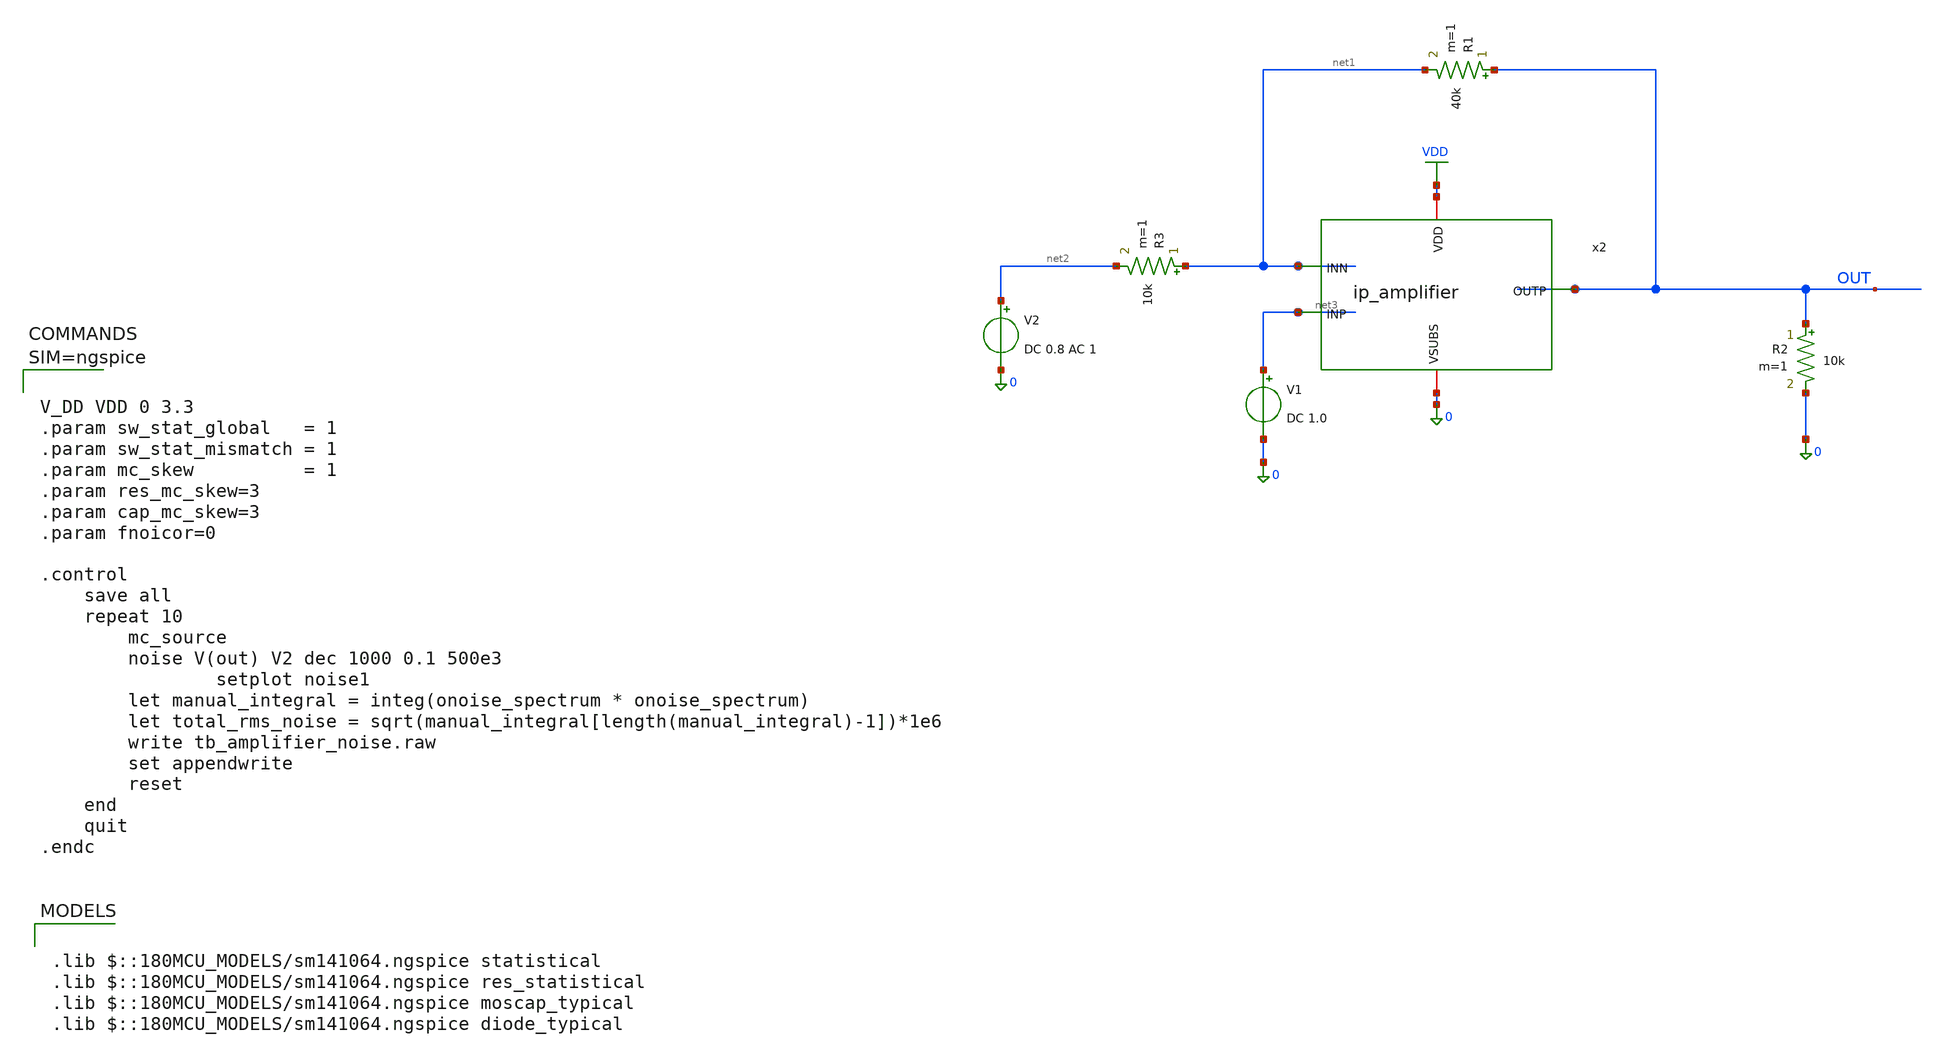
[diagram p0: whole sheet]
** sch_path: xschem/tb_amplifier_noise.sch
**.subckt tb_amplifier_noise
V2 net2 0 DC 0.8 AC 1
x2 VDD OUT net3 net1 0 ip_amplifier
R2 OUT 0 10k m=1
R1 OUT net1 40k m=1
R3 net1 net2 10k m=1
V1 net3 0 DC 1.0
**** begin user architecture code

.lib $::180MCU_MODELS/sm141064.ngspice statistical
.lib $::180MCU_MODELS/sm141064.ngspice res_statistical
.lib $::180MCU_MODELS/sm141064.ngspice moscap_typical
.lib $::180MCU_MODELS/sm141064.ngspice diode_typical




V_DD VDD 0 3.3
.param sw_stat_global   = 1
.param sw_stat_mismatch = 1
.param mc_skew          = 1
.param res_mc_skew=3
.param cap_mc_skew=3
.param fnoicor=0

.control
	save all
	repeat 10
		mc_source
		noise V(out) V2 dec 1000 0.1 500e3
                setplot noise1
		let manual_integral = integ(onoise_spectrum * onoise_spectrum)
		let total_rms_noise = sqrt(manual_integral[length(manual_integral)-1])*1e6
		write tb_amplifier_noise.raw
		set appendwrite
		reset
	end
	quit
.endc



**** end user architecture code
**.ends

* expanding   symbol:  ip_amplifier.sym # of pins=5
** sym_path: xschem/ip_amplifier.sym
** sch_path: xschem/ip_amplifier.sch
.subckt ip_amplifier VDD OUTP INP INN VSUBS
*.iopin VDD
*.iopin VSUBS
*.ipin INP
*.ipin INN
*.opin OUTP
XM1 net10 INP net8 VDD pfet_06v0 L=0.7u W=7.0u nf=1 ad='int((nf+1)/2) * W/nf * 0.18u' as='int((nf+2)/2) * W/nf * 0.18u'
+ pd='2*int((nf+1)/2) * (W/nf + 0.18u)' ps='2*int((nf+2)/2) * (W/nf + 0.18u)' nrd='0.18u / W' nrs='0.18u / W'
+ sa=0 sb=0 sd=0 m=3 par=3
XM2 net9 INN net8 VDD pfet_06v0 L=0.7u W=7.0u nf=1 ad='int((nf+1)/2) * W/nf * 0.18u' as='int((nf+2)/2) * W/nf * 0.18u'
+ pd='2*int((nf+1)/2) * (W/nf + 0.18u)' ps='2*int((nf+2)/2) * (W/nf + 0.18u)' nrd='0.18u / W' nrs='0.18u / W'
+ sa=0 sb=0 sd=0 m=3 par=3
XM5 net10 net1 VSUBS vsubs nfet_06v0 L=2u W=5u nf=1 ad='int((nf+1)/2) * W/nf * 0.18u' as='int((nf+2)/2) * W/nf * 0.18u'
+ pd='2*int((nf+1)/2) * (W/nf + 0.18u)' ps='2*int((nf+2)/2) * (W/nf + 0.18u)' nrd='0.18u / W' nrs='0.18u / W'
+ sa=0 sb=0 sd=0 m=1 par=1
XM6 net9 net1 VSUBS vsubs nfet_06v0 L=2u W=5u nf=1 ad='int((nf+1)/2) * W/nf * 0.18u' as='int((nf+2)/2) * W/nf * 0.18u'
+ pd='2*int((nf+1)/2) * (W/nf + 0.18u)' ps='2*int((nf+2)/2) * (W/nf + 0.18u)' nrd='0.18u / W' nrs='0.18u / W'
+ sa=0 sb=0 sd=0 m=1 par=1
XM3 net3 net1 VSUBS vsubs nfet_06v0 L=1u W=5u nf=1 ad='int((nf+1)/2) * W/nf * 0.18u' as='int((nf+2)/2) * W/nf * 0.18u'
+ pd='2*int((nf+1)/2) * (W/nf + 0.18u)' ps='2*int((nf+2)/2) * (W/nf + 0.18u)' nrd='0.18u / W' nrs='0.18u / W'
+ sa=0 sb=0 sd=0 m=5 par=5
XM4 net2 net1 VSUBS vsubs nfet_06v0 L=1u W=5u nf=1 ad='int((nf+1)/2) * W/nf * 0.18u' as='int((nf+2)/2) * W/nf * 0.18u'
+ pd='2*int((nf+1)/2) * (W/nf + 0.18u)' ps='2*int((nf+2)/2) * (W/nf + 0.18u)' nrd='0.18u / W' nrs='0.18u / W'
+ sa=0 sb=0 sd=0 m=1 par=1
XM7 net1 net1 net3 vsubs nfet_06v0 L=0.7u W=5u nf=1 ad='int((nf+1)/2) * W/nf * 0.18u' as='int((nf+2)/2) * W/nf * 0.18u'
+ pd='2*int((nf+1)/2) * (W/nf + 0.18u)' ps='2*int((nf+2)/2) * (W/nf + 0.18u)' nrd='0.18u / W' nrs='0.18u / W'
+ sa=0 sb=0 sd=0 m=7 par=7
XM8 net4 net1 net2 vsubs nfet_06v0 L=0.7u W=5u nf=1 ad='int((nf+1)/2) * W/nf * 0.18u' as='int((nf+2)/2) * W/nf * 0.18u'
+ pd='2*int((nf+1)/2) * (W/nf + 0.18u)' ps='2*int((nf+2)/2) * (W/nf + 0.18u)' nrd='0.18u / W' nrs='0.18u / W'
+ sa=0 sb=0 sd=0 m=7 par=7
XM9 net5 net7 VDD VDD pfet_06v0 L=1u W=6u nf=1 ad='int((nf+1)/2) * W/nf * 0.18u' as='int((nf+2)/2) * W/nf * 0.18u'
+ pd='2*int((nf+1)/2) * (W/nf + 0.18u)' ps='2*int((nf+2)/2) * (W/nf + 0.18u)' nrd='0.18u / W' nrs='0.18u / W'
+ sa=0 sb=0 sd=0 m=1 par=1
XM10 net6 net7 VDD VDD pfet_06v0 L=1u W=6u nf=1 ad='int((nf+1)/2) * W/nf * 0.18u' as='int((nf+2)/2) * W/nf * 0.18u'
+ pd='2*int((nf+1)/2) * (W/nf + 0.18u)' ps='2*int((nf+2)/2) * (W/nf + 0.18u)' nrd='0.18u / W' nrs='0.18u / W'
+ sa=0 sb=0 sd=0 m=1 par=1
XM11 net7 net7 net5 VDD pfet_06v0 L=0.7u W=7u nf=1 ad='int((nf+1)/2) * W/nf * 0.18u' as='int((nf+2)/2) * W/nf * 0.18u'
+ pd='2*int((nf+1)/2) * (W/nf + 0.18u)' ps='2*int((nf+2)/2) * (W/nf + 0.18u)' nrd='0.18u / W' nrs='0.18u / W'
+ sa=0 sb=0 sd=0 m=5 par=5
XM12 net8 net7 net6 VDD pfet_06v0 L=0.7u W=7u nf=1 ad='int((nf+1)/2) * W/nf * 0.18u' as='int((nf+2)/2) * W/nf * 0.18u'
+ pd='2*int((nf+1)/2) * (W/nf + 0.18u)' ps='2*int((nf+2)/2) * (W/nf + 0.18u)' nrd='0.18u / W' nrs='0.18u / W'
+ sa=0 sb=0 sd=0 m=5 par=5
XM13 net11 net1 net9 vsubs nfet_06v0 L=0.7u W=7u nf=1 ad='int((nf+1)/2) * W/nf * 0.18u' as='int((nf+2)/2) * W/nf * 0.18u'
+ pd='2*int((nf+1)/2) * (W/nf + 0.18u)' ps='2*int((nf+2)/2) * (W/nf + 0.18u)' nrd='0.18u / W' nrs='0.18u / W'
+ sa=0 sb=0 sd=0 m=1 par=1
XM14 COMP net1 net10 vsubs nfet_06v0 L=0.7u W=7u nf=1 ad='int((nf+1)/2) * W/nf * 0.18u' as='int((nf+2)/2) * W/nf * 0.18u'
+ pd='2*int((nf+1)/2) * (W/nf + 0.18u)' ps='2*int((nf+2)/2) * (W/nf + 0.18u)' nrd='0.18u / W' nrs='0.18u / W'
+ sa=0 sb=0 sd=0 m=1 par=1
XM15 net11 net11 VDD VDD pfet_06v0 L=0.7u W=7u nf=1 ad='int((nf+1)/2) * W/nf * 0.18u' as='int((nf+2)/2) * W/nf * 0.18u'
+ pd='2*int((nf+1)/2) * (W/nf + 0.18u)' ps='2*int((nf+2)/2) * (W/nf + 0.18u)' nrd='0.18u / W' nrs='0.18u / W'
+ sa=0 sb=0 sd=0 m=1 par=1
XM16 COMP net11 VDD VDD pfet_06v0 L=0.7u W=7u nf=1 ad='int((nf+1)/2) * W/nf * 0.18u' as='int((nf+2)/2) * W/nf * 0.18u'
+ pd='2*int((nf+1)/2) * (W/nf + 0.18u)' ps='2*int((nf+2)/2) * (W/nf + 0.18u)' nrd='0.18u / W' nrs='0.18u / W'
+ sa=0 sb=0 sd=0 m=1 par=1
XM17 OUTP COMP VDD VDD pfet_06v0 L=0.5u W=5u nf=1 ad='int((nf+1)/2) * W/nf * 0.18u' as='int((nf+2)/2) * W/nf * 0.18u'
+ pd='2*int((nf+1)/2) * (W/nf + 0.18u)' ps='2*int((nf+2)/2) * (W/nf + 0.18u)' nrd='0.18u / W' nrs='0.18u / W'
+ sa=0 sb=0 sd=0 m=12 par=12
XM18 OUTP net10 VSUBS vsubs nfet_06v0 L=0.7u W=5u nf=1 ad='int((nf+1)/2) * W/nf * 0.18u' as='int((nf+2)/2) * W/nf * 0.18u'
+ pd='2*int((nf+1)/2) * (W/nf + 0.18u)' ps='2*int((nf+2)/2) * (W/nf + 0.18u)' nrd='0.18u / W' nrs='0.18u / W'
+ sa=0 sb=0 sd=0 m=6 par=6
XR3 net1 net14 vsubs ppolyf_u_1k_6p0 r_width=1e-6 r_length=6e-6 m=1
XR6 net14 net13 vsubs ppolyf_u_1k_6p0 r_width=1e-6 r_length=6e-6 m=1
XR7 net13 net12 vsubs ppolyf_u_1k_6p0 r_width=1e-6 r_length=6e-6 m=1
XR8 net12 net15 vsubs ppolyf_u_1k_6p0 r_width=1e-6 r_length=4e-6 m=1
Vmeas VDD net15 0
Vmeas1 net7 net4 0
XC1 OUTP net16 cap_nmos_03v3 c_width=12e-6 c_length=18e-6 m=1
XC2 COMP net19 cap_nmos_03v3 c_width=12e-6 c_length=18e-6 m=1
XR12 net16 net17 vsubs ppolyf_u_1k_6p0 r_width=1e-6 r_length=5e-6 m=1
XR13 net17 COMP vsubs ppolyf_u_1k_6p0 r_width=1e-6 r_length=5e-6 m=1
XR15 OUTP net18 vsubs ppolyf_u_1k_6p0 r_width=1e-6 r_length=5e-6 m=1
XR16 net18 net19 vsubs ppolyf_u_1k_6p0 r_width=1e-6 r_length=5e-6 m=1
.ends

.GLOBAL VDD
.end
